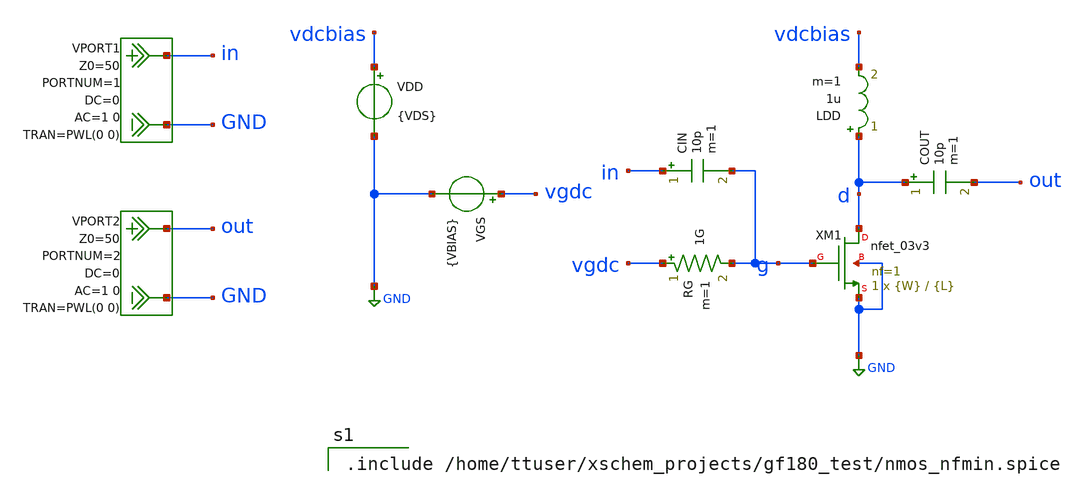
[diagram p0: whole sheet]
** sch_path: simulations/nfmin_sweeps/nfmin_jd_nmos.sch
**.subckt nfmin_jd_nmos
XM1 d g GND GND nfet_03v3 L={L} W={W} nf=1 ad='int((nf+1)/2) * W/nf * 0.18u' as='int((nf+2)/2) * W/nf * 0.18u'
+ pd='2*int((nf+1)/2) * (W/nf + 0.18u)' ps='2*int((nf+2)/2) * (W/nf + 0.18u)' nrd='0.18u / W' nrs='0.18u / W'
+ sa=0 sb=0 sd=0 m=1
VGS vgdc GND {VBIAS}
VDD vdcbias GND {VDS}
LDD d vdcbias 1u m=1
RG vgdc g 1G m=1
COUT d out 10p m=1
VPORT1 in GND DC 0 AC 1 0 portnum 1 z0 50 PWL(0 0)
VPORT2 out GND DC 0 AC 1 0 portnum 2 z0 50 PWL(0 0)
CIN in g 10p m=1
**** begin user architecture code

.include /home/ttuser/xschem_projects/gf180_test/nmos_nfmin.spice

**** end user architecture code
**.ends
.GLOBAL GND
.end
